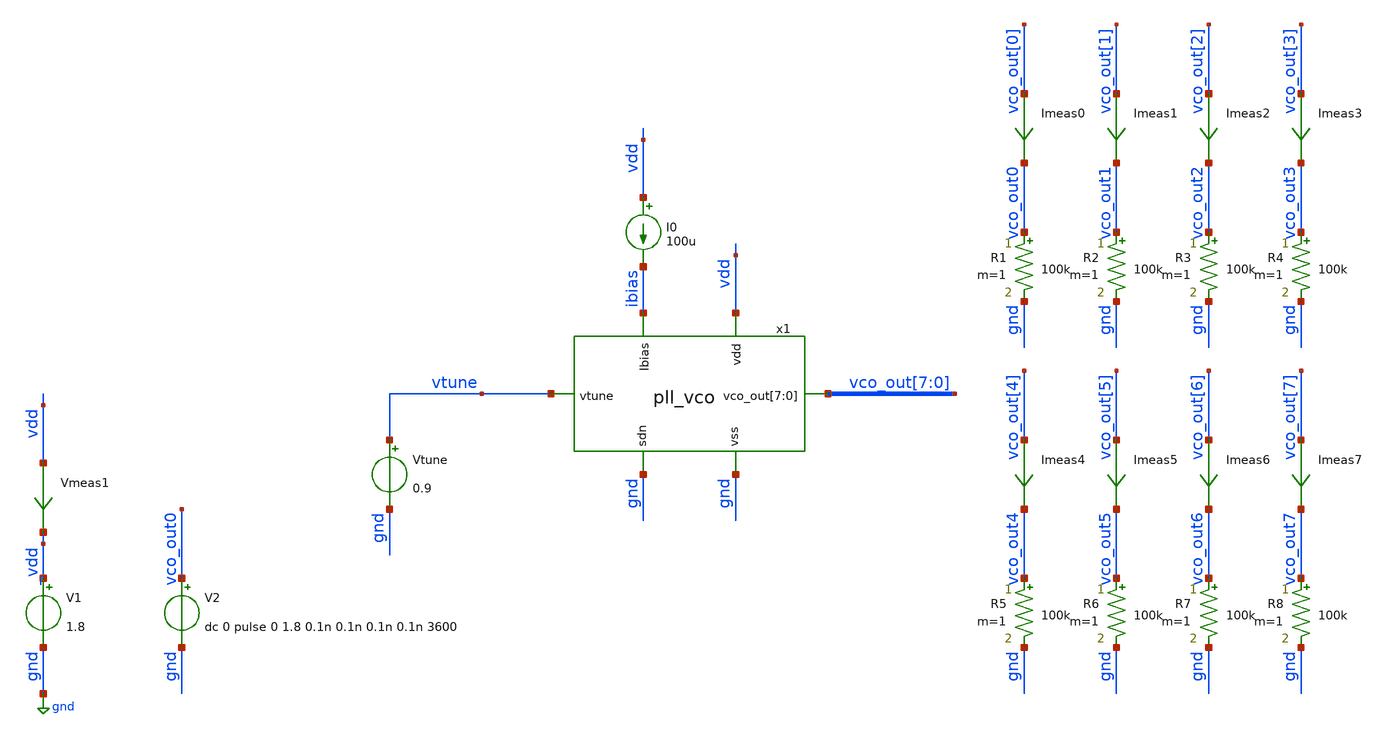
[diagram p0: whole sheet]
** sch_path: pll/pll_vco/simulation/pll_vco_tb.sch
**.subckt pll_vco_tb
V1 _vdd gnd 1.8
I0 vdd ibias 100u
Vmeas1 vdd _vdd 0
.save i(vmeas1)
Vtune vtune gnd 0.9
R1 vco_out0 gnd 100k m=1
R2 vco_out1 gnd 100k m=1
R3 vco_out2 gnd 100k m=1
R4 vco_out3 gnd 100k m=1
R5 vco_out4 gnd 100k m=1
R6 vco_out5 gnd 100k m=1
R7 vco_out6 gnd 100k m=1
R8 vco_out7 gnd 100k m=1
Imeas0 vco_out[0] vco_out0 0
.save i(imeas0)
Imeas1 vco_out[1] vco_out1 0
.save i(imeas1)
Imeas2 vco_out[2] vco_out2 0
.save i(imeas2)
Imeas3 vco_out[3] vco_out3 0
.save i(imeas3)
Imeas4 vco_out[4] vco_out4 0
.save i(imeas4)
Imeas5 vco_out[5] vco_out5 0
.save i(imeas5)
Imeas6 vco_out[6] vco_out6 0
.save i(imeas6)
Imeas7 vco_out[7] vco_out7 0
.save i(imeas7)
V2 vco_out0 gnd dc 0 pulse 0 1.8 0.1n 0.1n 0.1n 0.1n 3600
x1 vdd vtune vco_out[7] vco_out[6] vco_out[5] vco_out[4] vco_out[3] vco_out[2] vco_out[1] vco_out[0]
+ ibias gnd gnd pll_vco
**** begin user architecture code



.option savecurrents
.option rshunt = 1e12
.option gmin = 1e-24
*.option method=Gear
*.option chgtol=1e-12

.option method=gear
*.option abstol=1e-12
.option vntol=1e-6
*.option chgtol=1e-16
.option reltol=1e-6
*.option trtol=10


*.model switch1 aswitch(cntl_off=0.0 cntl_on=0.1 r_off=1e12 r_on=1.0 log=TRUE)
.model sw SW (ron=0.1 roff=1e12 vt=0.5 vh=0)

.control
* Main Amplifier
** Main Core OP params
save i(@m.x1.xm1.msky130_fd_pr__nfet_01v8[id])
save @m.x1.xm1.msky130_fd_pr__nfet_01v8[gm]
save v(@m.x1.xm1.msky130_fd_pr__nfet_01v8[vds])
save v(@m.x1.xm1.msky130_fd_pr__nfet_01v8[vgs])
save v(@m.x1.xm1.msky130_fd_pr__nfet_01v8[vth])
save v(@m.x1.xm1.msky130_fd_pr__nfet_01v8[vdsat])


* #################################################################
* #
* #                         OPERATING POINT
* #
* #################################################################
save all
save v(vin_p)
save v(vin_n)
save v(vg_p)
save v(vg_n)
save v(vout_p)
save v(vout_n)

op
set filetype=binary
write pll_vco_tb.raw all

* #################################################################
* #
* #                 TRANSIENT OSCILATION REGIME
* #
* #################################################################
reset
save all
save v(vco_out)
save v(vco_out<0>) v(vco_out<1>) v(vco_out<2>) v(vco_out<3>) v(vco_out<4>) v(vco_out<5>)
+ v(vco_out<6>) v(vco_out<7>)
save v(vtune)

*.ic v(vco_out<0>)=1.8 v(vco_out<4>)=0
*.ic v(vco_out0)=1.8 v(vco_out4)=0
tran 1n 10n 0
set filetype=ascii
write pll_vco_tb_tran.raw all

plot v(vco_out0) v(vco_out1) v(vco_out2) v(vco_out3) v(vco_out4) v(vco_out5) v(vco_out6) v(vco_out7)
plot v(vtune)
plot v(vco_out0)

.endc



.options wnflag=1
.include $::SKYWATER_MODELS/cells/nfet_01v8/sky130_fd_pr__nfet_01v8__tt.corner.spice
.include $::SKYWATER_MODELS/cells/nfet_01v8_lvt/sky130_fd_pr__nfet_01v8_lvt__tt.corner.spice
.include $::SKYWATER_MODELS/cells/pfet_01v8/sky130_fd_pr__pfet_01v8__tt.corner.spice
.include $::SKYWATER_MODELS/cells/nfet_03v3_nvt/sky130_fd_pr__nfet_03v3_nvt__tt.corner.spice
.include $::SKYWATER_MODELS/cells/nfet_05v0_nvt/sky130_fd_pr__nfet_05v0_nvt__tt.corner.spice
.include $::SKYWATER_MODELS/cells/esd_nfet_01v8/sky130_fd_pr__esd_nfet_01v8__tt.corner.spice
.include $::SKYWATER_MODELS/cells/pfet_01v8_lvt/sky130_fd_pr__pfet_01v8_lvt__tt.corner.spice
.include $::SKYWATER_MODELS/cells/pfet_01v8_hvt/sky130_fd_pr__pfet_01v8_hvt__tt.corner.spice
.include $::SKYWATER_MODELS/cells/esd_pfet_g5v0d10v5/sky130_fd_pr__esd_pfet_g5v0d10v5__tt.corner.spice
.include $::SKYWATER_MODELS/cells/pfet_g5v0d10v5/sky130_fd_pr__pfet_g5v0d10v5__tt.corner.spice
.include $::SKYWATER_MODELS/cells/pfet_g5v0d16v0/sky130_fd_pr__pfet_g5v0d16v0__tt.corner.spice
.include $::SKYWATER_MODELS/cells/nfet_g5v0d10v5/sky130_fd_pr__nfet_g5v0d10v5__tt.corner.spice
.include $::SKYWATER_MODELS/cells/nfet_g5v0d16v0/sky130_fd_pr__nfet_g5v0d16v0__tt_discrete.corner.spice
.include $::SKYWATER_MODELS/cells/esd_nfet_g5v0d10v5/sky130_fd_pr__esd_nfet_g5v0d10v5__tt.corner.spice
.include $::SKYWATER_MODELS/models/corners/tt/nonfet.spice
* Mismatch parameters
.include $::SKYWATER_MODELS/cells/nfet_01v8/sky130_fd_pr__nfet_01v8__mismatch.corner.spice
.include $::SKYWATER_MODELS/cells/pfet_01v8/sky130_fd_pr__pfet_01v8__mismatch.corner.spice
.include $::SKYWATER_MODELS/cells/nfet_01v8_lvt/sky130_fd_pr__nfet_01v8_lvt__mismatch.corner.spice
.include $::SKYWATER_MODELS/cells/pfet_01v8_lvt/sky130_fd_pr__pfet_01v8_lvt__mismatch.corner.spice
.include $::SKYWATER_MODELS/cells/pfet_01v8_hvt/sky130_fd_pr__pfet_01v8_hvt__mismatch.corner.spice
.include $::SKYWATER_MODELS/cells/nfet_g5v0d10v5/sky130_fd_pr__nfet_g5v0d10v5__mismatch.corner.spice
.include $::SKYWATER_MODELS/cells/pfet_g5v0d10v5/sky130_fd_pr__pfet_g5v0d10v5__mismatch.corner.spice
.include $::SKYWATER_MODELS/cells/nfet_05v0_nvt/sky130_fd_pr__nfet_05v0_nvt__mismatch.corner.spice
.include $::SKYWATER_MODELS/cells/nfet_03v3_nvt/sky130_fd_pr__nfet_03v3_nvt__mismatch.corner.spice
* Resistor$::SKYWATER_MODELS/Capacitor
.include $::SKYWATER_MODELS/models/r+c/res_typical__cap_typical.spice
.include $::SKYWATER_MODELS/models/r+c/res_typical__cap_typical__lin.spice
* Special cells
.include $::SKYWATER_MODELS/models/corners/tt/specialized_cells.spice
* All models
.include $::SKYWATER_MODELS/models/all.spice
* Corner
.include $::SKYWATER_MODELS/models/corners/tt/rf.spice

**** end user architecture code
**.ends

* expanding   symbol:  ../xschem/pll_vco.sym # of pins=6
** sym_path: pll/pll_vco/xschem/pll_vco.sym
** sch_path: pll/pll_vco/xschem/pll_vco.sch
.subckt pll_vco vdd vtune vco_out[7] vco_out[6] vco_out[5] vco_out[4] vco_out[3] vco_out[2]
+ vco_out[1] vco_out[0] Ibias vss sdn
*.iopin vss
*.iopin vdd
*.iopin vtune
*.iopin Ibias
*.opin vco_out[0],vco_out[1],vco_out[2],vco_out[3],vco_out[4],vco_out[5],vco_out[6],vco_out[7]
*.iopin sdn
**** begin user architecture code


.control
save i(@m.${path}xm1.msky130_fd_pr__nfet_01v8[id])
save @m.${path}xm1.msky130_fd_pr__nfet_01v8[gm]
save v(@m.${path}xm1.msky130_fd_pr__nfet_01v8[vds])
save v(@m.${path}xm1.msky130_fd_pr__nfet_01v8[vgs])
save v(@m.${path}xm1.msky130_fd_pr__nfet_01v8[vth])
save v(@m.${path}xm1.msky130_fd_pr__nfet_01v8[vdsat])

save i(@m.${path}xm2.msky130_fd_pr__nfet_01v8[id])
save @m.${path}xm2.msky130_fd_pr__nfet_01v8[gm]
save v(@m.${path}xm2.msky130_fd_pr__nfet_01v8[vds])
save v(@m.${path}xm2.msky130_fd_pr__nfet_01v8[vgs])
save v(@m.${path}xm2.msky130_fd_pr__nfet_01v8[vth])
save v(@m.${path}xm2.msky130_fd_pr__nfet_01v8[vdsat])
.endc


**** end user architecture code
XM0 Ibias Ibias vss vss sky130_fd_pr__nfet_01v8 L=0.3 W=10 nf=1 ad='int((nf+1)/2) * W/nf * 0.29' as='int((nf+2)/2) * W/nf * 0.29'
+ pd='2*int((nf+1)/2) * (W/nf + 0.29)' ps='2*int((nf+2)/2) * (W/nf + 0.29)' nrd='0.29 / W' nrs='0.29 / W'
+ sa=0 sb=0 sd=0 mult=1 m=1
x5[0] phi[0] vss vss vdd vdd net1[7] sky130_fd_sc_hs__inv_1
x5[1] phi[1] vss vss vdd vdd net1[6] sky130_fd_sc_hs__inv_1
x5[2] phi[2] vss vss vdd vdd net1[5] sky130_fd_sc_hs__inv_1
x5[3] phi[3] vss vss vdd vdd net1[4] sky130_fd_sc_hs__inv_1
x5[4] phi[4] vss vss vdd vdd net1[3] sky130_fd_sc_hs__inv_1
x5[5] phi[5] vss vss vdd vdd net1[2] sky130_fd_sc_hs__inv_1
x5[6] phi[6] vss vss vdd vdd net1[1] sky130_fd_sc_hs__inv_1
x5[7] phi[7] vss vss vdd vdd net1[0] sky130_fd_sc_hs__inv_1
x6[0] net1[7] vss vss vdd vdd net2[7] sky130_fd_sc_hs__inv_2
x6[1] net1[6] vss vss vdd vdd net2[6] sky130_fd_sc_hs__inv_2
x6[2] net1[5] vss vss vdd vdd net2[5] sky130_fd_sc_hs__inv_2
x6[3] net1[4] vss vss vdd vdd net2[4] sky130_fd_sc_hs__inv_2
x6[4] net1[3] vss vss vdd vdd net2[3] sky130_fd_sc_hs__inv_2
x6[5] net1[2] vss vss vdd vdd net2[2] sky130_fd_sc_hs__inv_2
x6[6] net1[1] vss vss vdd vdd net2[1] sky130_fd_sc_hs__inv_2
x6[7] net1[0] vss vss vdd vdd net2[0] sky130_fd_sc_hs__inv_2
x7[0] net2[7] vss vss vdd vdd vco_out[0] sky130_fd_sc_hs__inv_4
x7[1] net2[6] vss vss vdd vdd vco_out[1] sky130_fd_sc_hs__inv_4
x7[2] net2[5] vss vss vdd vdd vco_out[2] sky130_fd_sc_hs__inv_4
x7[3] net2[4] vss vss vdd vdd vco_out[3] sky130_fd_sc_hs__inv_4
x7[4] net2[3] vss vss vdd vdd vco_out[4] sky130_fd_sc_hs__inv_4
x7[5] net2[2] vss vss vdd vdd vco_out[5] sky130_fd_sc_hs__inv_4
x7[6] net2[1] vss vss vdd vdd vco_out[6] sky130_fd_sc_hs__inv_4
x7[7] net2[0] vss vss vdd vdd vco_out[7] sky130_fd_sc_hs__inv_4
x1 phi[0] phi[4] phi[7] phi[3] vdd vtune Ibias vss sdn pll_vco_cell
x2 phi[1] phi[5] phi[0] phi[4] vdd vtune Ibias vss sdn pll_vco_cell
x3 phi[2] phi[6] phi[1] phi[5] vdd vtune Ibias vss sdn pll_vco_cell
x4 phi[3] phi[7] phi[2] phi[6] vdd vtune Ibias vss sdn pll_vco_cell
.ends


* expanding   symbol:  pll_vco_cell/xschem/pll_vco_cell.sym # of pins=9
** sym_path: pll/pll_vco_cell/xschem/pll_vco_cell.sym
** sch_path: pll/pll_vco_cell/xschem/pll_vco_cell.sch
.subckt pll_vco_cell out_n out_p in_p in_n vdd vtune vbias vss sdn
*.iopin vss
*.iopin vdd
*.ipin in_p
*.ipin in_n
*.iopin vbias
*.opin out_n
*.opin out_p
*.ipin vtune
*.ipin sdn
**** begin user architecture code


*.control
*save i(@m.${path}xm1.msky130_fd_pr__nfet_01v8[id])
*save @m.${path}xm1.msky130_fd_pr__nfet_01v8[gm]
*save v(@m.${path}xm1.msky130_fd_pr__nfet_01v8[vds])
*save v(@m.${path}xm1.msky130_fd_pr__nfet_01v8[vgs])
*save v(@m.${path}xm1.msky130_fd_pr__nfet_01v8[vth])
*save v(@m.${path}xm1.msky130_fd_pr__nfet_01v8[vdsat])

*save i(@m.${path}xm2.msky130_fd_pr__nfet_01v8[id])
*save @m.${path}xm2.msky130_fd_pr__nfet_01v8[gm]
*save v(@m.${path}xm2.msky130_fd_pr__nfet_01v8[vds])
*save v(@m.${path}xm2.msky130_fd_pr__nfet_01v8[vgs])
*save v(@m.${path}xm2.msky130_fd_pr__nfet_01v8[vth])
*save v(@m.${path}xm2.msky130_fd_pr__nfet_01v8[vdsat])
*.endc


**** end user architecture code
XM3 net1 vbias vss vss sky130_fd_pr__nfet_01v8 L=0.3 W=60 nf=1 ad='int((nf+1)/2) * W/nf * 0.29' as='int((nf+2)/2) * W/nf * 0.29'
+ pd='2*int((nf+1)/2) * (W/nf + 0.29)' ps='2*int((nf+2)/2) * (W/nf + 0.29)' nrd='0.29 / W' nrs='0.29 / W'
+ sa=0 sb=0 sd=0 mult=4 m=4
XM10 vbias sdn vss vss sky130_fd_pr__nfet_01v8 L=0.15 W=0.5 nf=1 ad='int((nf+1)/2) * W/nf * 0.29' as='int((nf+2)/2) * W/nf * 0.29'
+ pd='2*int((nf+1)/2) * (W/nf + 0.29)' ps='2*int((nf+2)/2) * (W/nf + 0.29)' nrd='0.29 / W' nrs='0.29 / W'
+ sa=0 sb=0 sd=0 mult=1 m=1
x1 sdn vss vss vdd vdd net2 sky130_fd_sc_hd__inv_1
x2 sdn vss vss vdd vdd net3 sky130_fd_sc_hd__inv_1
XM4 out_n out_n vdd vdd sky130_fd_pr__pfet_01v8 L=0.15 W=8 nf=1 ad='int((nf+1)/2) * W/nf * 0.29' as='int((nf+2)/2) * W/nf * 0.29'
+ pd='2*int((nf+1)/2) * (W/nf + 0.29)' ps='2*int((nf+2)/2) * (W/nf + 0.29)' nrd='0.29 / W' nrs='0.29 / W'
+ sa=0 sb=0 sd=0 mult=1 m=1
XM5 out_p out_p vdd vdd sky130_fd_pr__pfet_01v8 L=0.15 W=8 nf=1 ad='int((nf+1)/2) * W/nf * 0.29' as='int((nf+2)/2) * W/nf * 0.29'
+ pd='2*int((nf+1)/2) * (W/nf + 0.29)' ps='2*int((nf+2)/2) * (W/nf + 0.29)' nrd='0.29 / W' nrs='0.29 / W'
+ sa=0 sb=0 sd=0 mult=1 m=1
XM7 out_p out_n vdd vdd sky130_fd_pr__pfet_01v8 L=0.15 W=16 nf=1 ad='int((nf+1)/2) * W/nf * 0.29' as='int((nf+2)/2) * W/nf * 0.29'
+ pd='2*int((nf+1)/2) * (W/nf + 0.29)' ps='2*int((nf+2)/2) * (W/nf + 0.29)' nrd='0.29 / W' nrs='0.29 / W'
+ sa=0 sb=0 sd=0 mult=1 m=1
XM6 out_n out_p vdd vdd sky130_fd_pr__pfet_01v8 L=0.15 W=16 nf=1 ad='int((nf+1)/2) * W/nf * 0.29' as='int((nf+2)/2) * W/nf * 0.29'
+ pd='2*int((nf+1)/2) * (W/nf + 0.29)' ps='2*int((nf+2)/2) * (W/nf + 0.29)' nrd='0.29 / W' nrs='0.29 / W'
+ sa=0 sb=0 sd=0 mult=1 m=1
XM8 out_n net2 vdd vdd sky130_fd_pr__pfet_01v8 L=0.15 W=0.5 nf=1 ad='int((nf+1)/2) * W/nf * 0.29' as='int((nf+2)/2) * W/nf * 0.29'
+ pd='2*int((nf+1)/2) * (W/nf + 0.29)' ps='2*int((nf+2)/2) * (W/nf + 0.29)' nrd='0.29 / W' nrs='0.29 / W'
+ sa=0 sb=0 sd=0 mult=1 m=1
XM9 out_p net3 vdd vdd sky130_fd_pr__pfet_01v8 L=0.15 W=0.5 nf=1 ad='int((nf+1)/2) * W/nf * 0.29' as='int((nf+2)/2) * W/nf * 0.29'
+ pd='2*int((nf+1)/2) * (W/nf + 0.29)' ps='2*int((nf+2)/2) * (W/nf + 0.29)' nrd='0.29 / W' nrs='0.29 / W'
+ sa=0 sb=0 sd=0 mult=1 m=1
XM1 out_n in_p net1 vss sky130_fd_pr__nfet_01v8 L=0.15 W=16 nf=1 ad='int((nf+1)/2) * W/nf * 0.29' as='int((nf+2)/2) * W/nf * 0.29'
+ pd='2*int((nf+1)/2) * (W/nf + 0.29)' ps='2*int((nf+2)/2) * (W/nf + 0.29)' nrd='0.29 / W' nrs='0.29 / W'
+ sa=0 sb=0 sd=0 mult=1 m=1
XM2 out_p in_n net1 vss sky130_fd_pr__nfet_01v8 L=0.15 W=16 nf=1 ad='int((nf+1)/2) * W/nf * 0.29' as='int((nf+2)/2) * W/nf * 0.29'
+ pd='2*int((nf+1)/2) * (W/nf + 0.29)' ps='2*int((nf+2)/2) * (W/nf + 0.29)' nrd='0.29 / W' nrs='0.29 / W'
+ sa=0 sb=0 sd=0 mult=1 m=1
XC1 out_n vtune vss sky130_fd_pr__cap_var_lvt W=7 L=4 VM=3 m=3
XC2 out_p vtune vss sky130_fd_pr__cap_var_lvt W=7 L=4 VM=3 m=3
.ends

.GLOBAL gnd
.end
